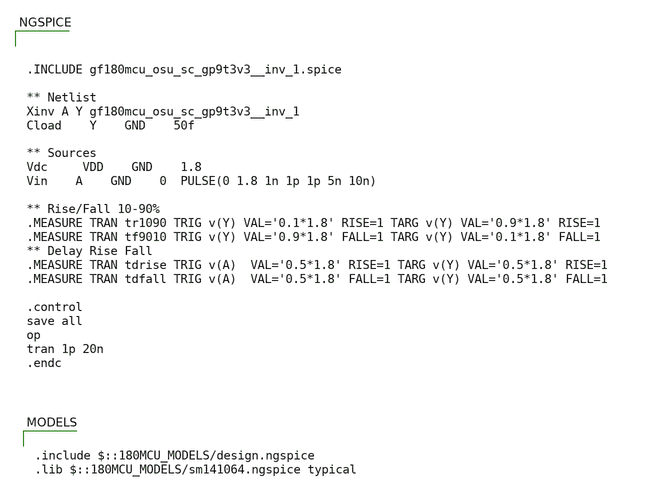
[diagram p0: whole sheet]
** sch_path: examples/TB_inv1.sch
**.subckt TB_inv1
**** begin user architecture code



.INCLUDE gf180mcu_osu_sc_gp9t3v3__inv_1.spice

** Netlist
Xinv A Y gf180mcu_osu_sc_gp9t3v3__inv_1
Cload	Y	GND	50f

** Sources
Vdc 	VDD	GND	1.8
Vin	A	GND	0  PULSE(0 1.8 1n 1p 1p 5n 10n)

** Rise/Fall 10-90%
.MEASURE TRAN tr1090 TRIG v(Y) VAL='0.1*1.8' RISE=1 TARG v(Y) VAL='0.9*1.8' RISE=1
.MEASURE TRAN tf9010 TRIG v(Y) VAL='0.9*1.8' FALL=1 TARG v(Y) VAL='0.1*1.8' FALL=1
** Delay Rise Fall
.MEASURE TRAN tdrise TRIG v(A)  VAL='0.5*1.8' RISE=1 TARG v(Y) VAL='0.5*1.8' RISE=1
.MEASURE TRAN tdfall TRIG v(A)  VAL='0.5*1.8' FALL=1 TARG v(Y) VAL='0.5*1.8' FALL=1

.control
save all
op
tran 1p 20n
.endc



.include $::180MCU_MODELS/design.ngspice
.lib $::180MCU_MODELS/sm141064.ngspice typical

**** end user architecture code
**.ends
.end
